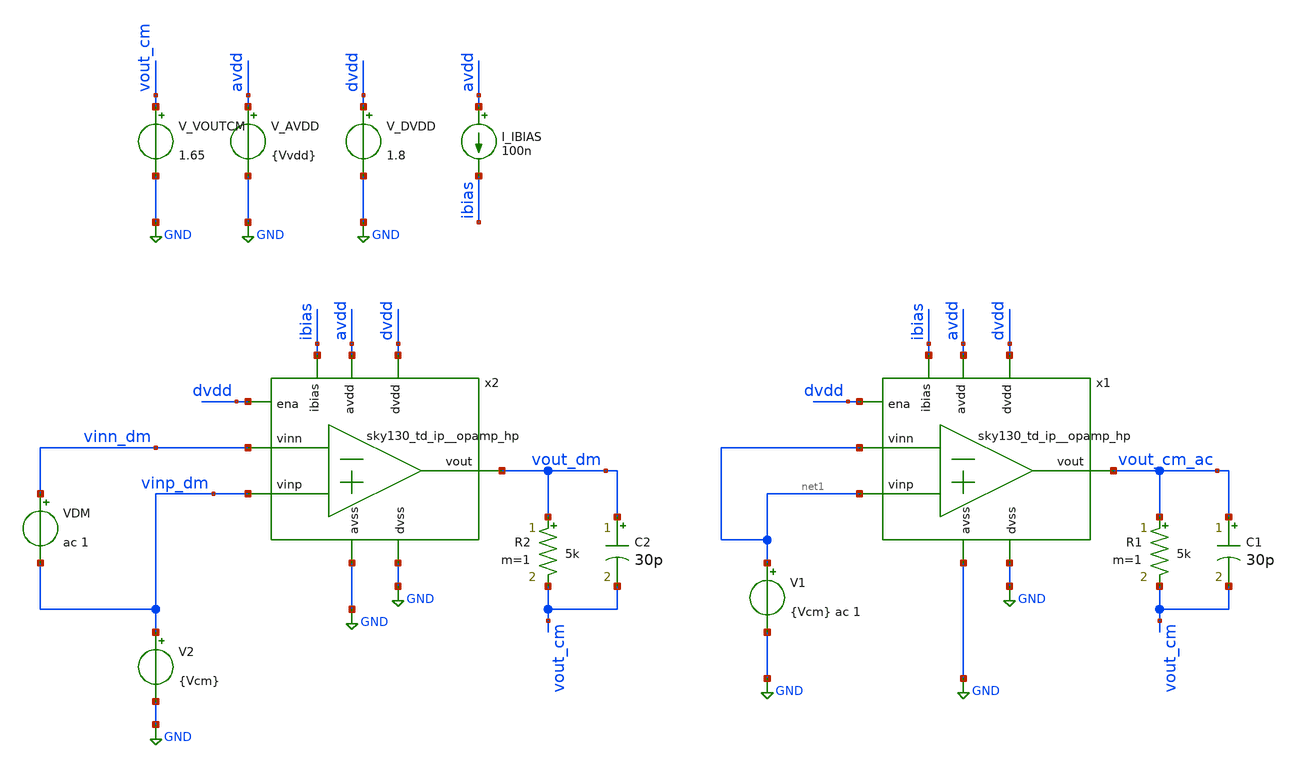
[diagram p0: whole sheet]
** sch_path: IP_open_sources/cmrr.sch
**.subckt cmrr
x1 avdd vout_cm_ac ibias net1 net1 GND dvdd GND dvdd sky130_td_ip__opamp_hp
V_AVDD avdd GND {Vvdd}
.save i(v_avdd)
V_DVDD dvdd GND 1.8
.save i(v_dvdd)
I_IBIAS avdd ibias 100n
R1 vout_cm_ac vout_cm 5k m=1
C1 vout_cm_ac vout_cm 30p m=1
V_VOUTCM vout_cm GND 1.65
.save i(v_voutcm)
V1 net1 GND {Vcm} ac 1
x2 avdd vout_dm ibias vinn_dm vinp_dm GND dvdd GND dvdd sky130_td_ip__opamp_hp
R2 vout_dm vout_cm 5k m=1
C2 vout_dm vout_cm 30p m=1
VDM vinn_dm vinp_dm ac 1
V2 vinp_dm GND {Vcm}
**** begin user architecture code


.control
save all

* Calculate input offset voltage
alter @VDM[pwl] = [ 0 -10m 10 10m ]
tran 10m 10
run
let vid = v(vinn_dm) - v(vinp_dm)
let vout = v(vout_dm)

meas tran input_offset_voltage FIND vid WHEN vout=1.65


alter @VDM[pwl] = [ 0 0 ]
alter VDM dc = $&input_offset_voltage
alter VDM ac = 1

* Run AC sweep from 1Hz to 1GHz
AC DEC 100 1 1000000000
run

* Get DC gain in DBs.
let adm_db = db(vout_dm)
let acm_db = db(vout_cm_ac)
let cmrr_db = adm_db - acm_db

meas AC cmrr_dc FIND cmrr_db AT=1
meas AC cmrr_10k FIND cmrr_db AT=10K

echo
echo ===================================
echo CMRR characterization results:
echo - CMRR @ 1 Hz: $&cmrr_dc
echo - CMRR @ 10 kHz: $&cmrr_10k
echo ===================================

echo $&cmrr_dc $&cmrr_10k > {simpath}/{filename}_{N}.data
quit
.endc




* CACE gensim simulation file {filename}_{N}
* Generated by CACE gensim, Efabless Corporation (c) 2023
* Find the power supply rejection ratio of the amplifier

.include /home/etienne/test_xschem_sky130/IFSET/sky130_td_ip__opamp_hp.sym

.lib {PDK_ROOT}/{PDK}/libs.tech/combined/sky130.lib.spice {corner}

.option TEMP={temperature}
* Flag unsafe operating conditions (exceeds models' specified limits)
.option warn=1
.option SEED=[{seed=12345} + {iterations=0}]


**** end user architecture code
**.ends
.GLOBAL GND
.end
